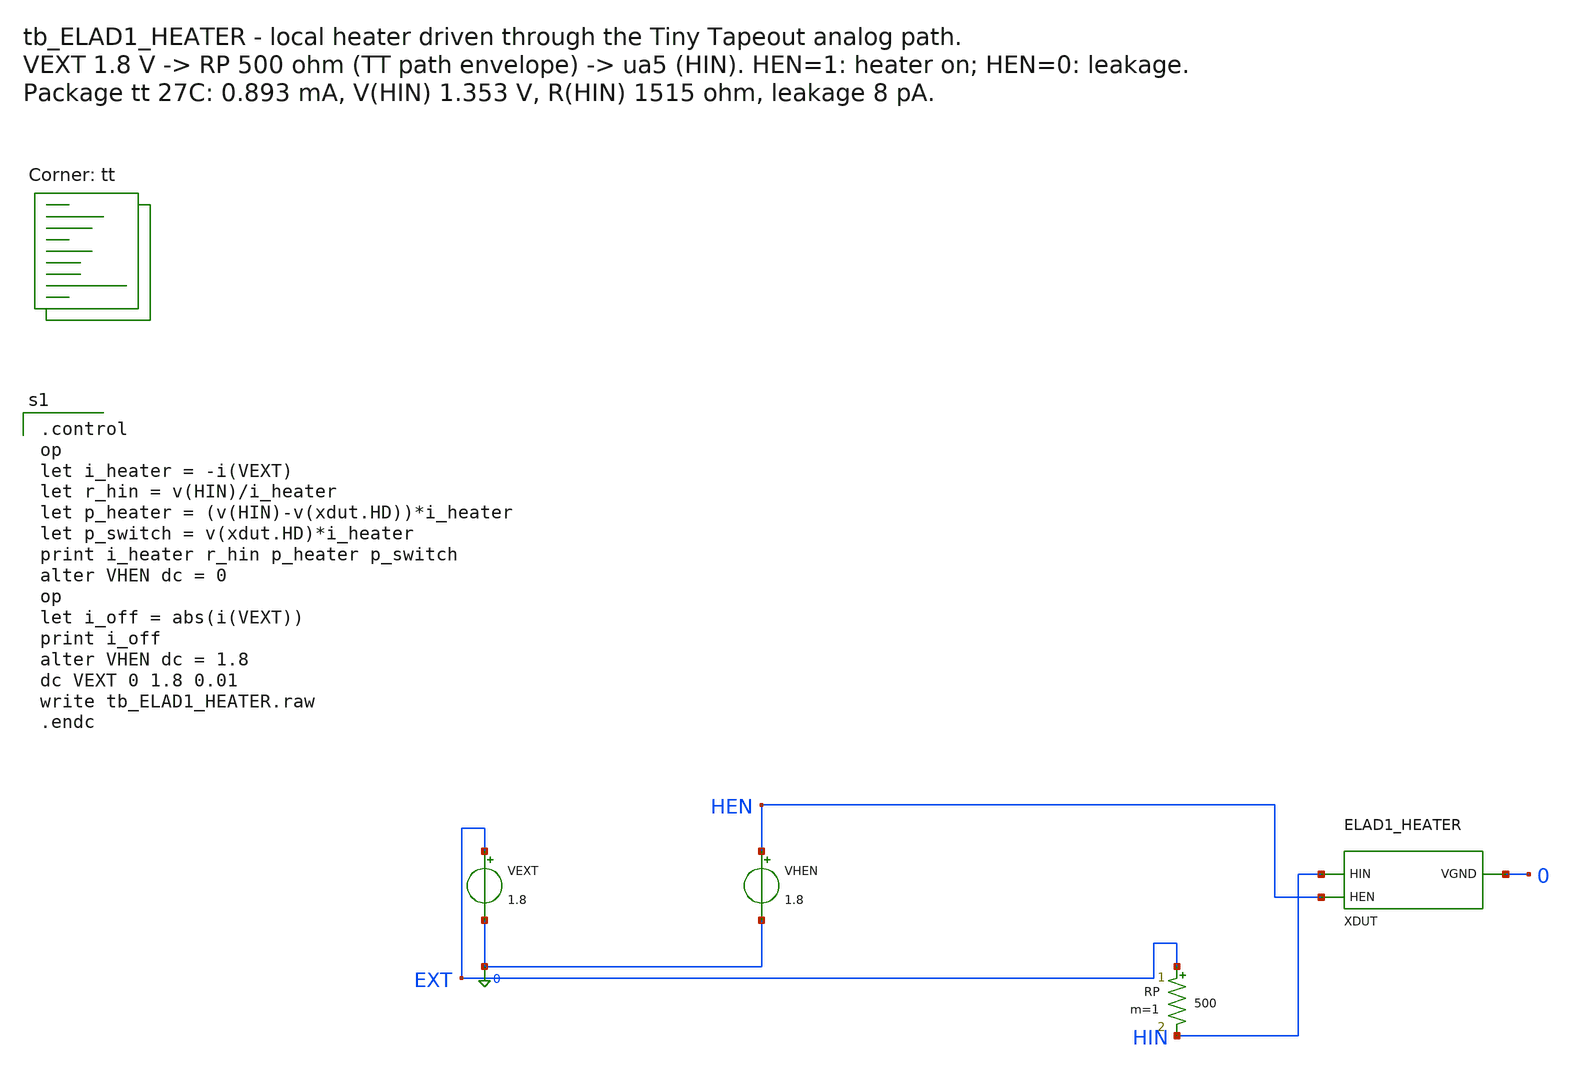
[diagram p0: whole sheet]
** sch_path: cells/ELAD1_HEATER/schematic/tb_ELAD1_HEATER.sch
**.subckt tb_ELAD1_HEATER
VEXT EXT 0 1.8
RP EXT HIN 500 m=1
VHEN HEN 0 1.8
XDUT HIN HEN 0 ELAD1_HEATER
**** begin user architecture code

.control
op
let i_heater = -i(VEXT)
let r_hin = v(HIN)/i_heater
let p_heater = (v(HIN)-v(xdut.HD))*i_heater
let p_switch = v(xdut.HD)*i_heater
print i_heater r_hin p_heater p_switch
alter VHEN dc = 0
op
let i_off = abs(i(VEXT))
print i_off
alter VHEN dc = 1.8
dc VEXT 0 1.8 0.01
write tb_ELAD1_HEATER.raw
.endc

.lib $::SKYWATER_MODELS/sky130.lib.spice tt
**** end user architecture code
**.ends

* expanding   symbol:  ELAD1_HEATER.sym # of pins=3
** sym_path: cells/ELAD1_HEATER/schematic/ELAD1_HEATER.sym
** sch_path: cells/ELAD1_HEATER/schematic/ELAD1_HEATER.sch
.subckt ELAD1_HEATER HIN HEN VGND
*.iopin HIN
*.iopin HEN
*.iopin VGND
XRH0 HIN HD VGND sky130_fd_pr__res_high_po W=5.73 L=52.9 mult=1 m=1
XRH1 HIN HD VGND sky130_fd_pr__res_high_po W=5.73 L=52.9 mult=1 m=1
XMSW HD HEN VGND VGND sky130_fd_pr__nfet_01v8 L=0.15 W=40 nf=1 ad='int((1 + 1)/2) * 40 / 1 * 0.29' as='int((1 + 2)/2) * 40 / 1 * 0.29'
+ pd='2*int((1 + 1)/2) * (40 / 1 + 0.29)' ps='2*int((1 + 2)/2) * (40 / 1 + 0.29)' nrd='0.29 / 40 ' nrs='0.29 / 40 '
+ sa=0 sb=0 sd=0 mult=1 m=1
.ends

.GLOBAL VGND
.end
